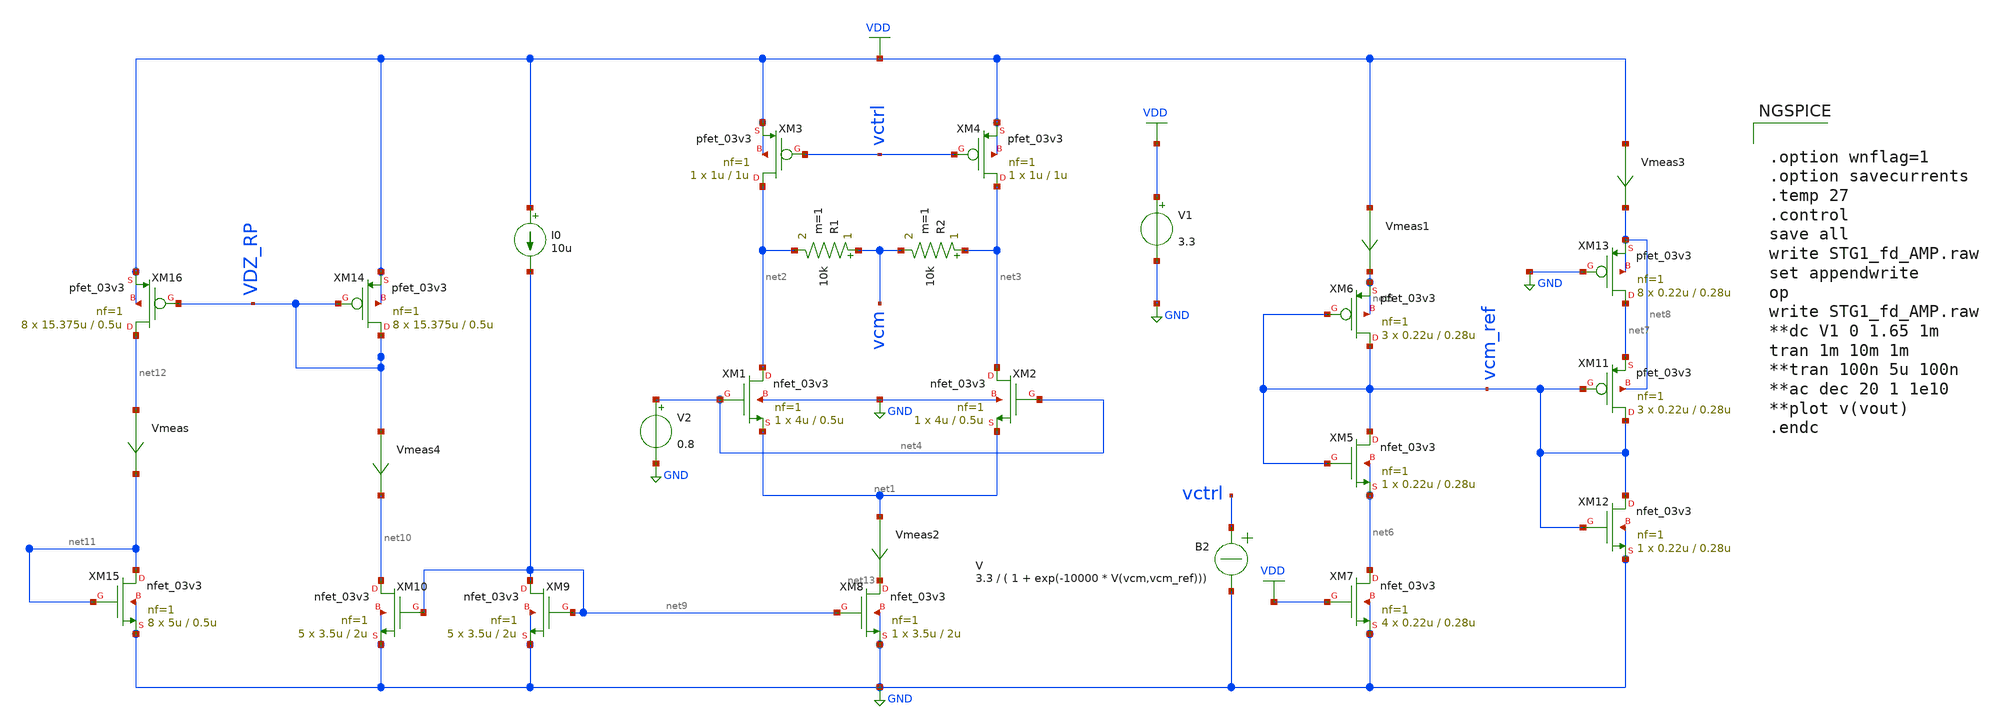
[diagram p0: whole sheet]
** sch_path: Design_Files/TB_ideal/STG1_fd_AMP.sch
**.subckt STG1_fd_AMP
XM1 net2 net4 net1 GND nfet_03v3 L=0.5u W=4u nf=1 ad='int((nf+1)/2) * W/nf * 0.18u' as='int((nf+2)/2) * W/nf * 0.18u'
+ pd='2*int((nf+1)/2) * (W/nf + 0.18u)' ps='2*int((nf+2)/2) * (W/nf + 0.18u)' nrd='0.18u / W' nrs='0.18u / W'
+ sa=0 sb=0 sd=0 m=1
XM2 net3 net4 net1 GND nfet_03v3 L=0.5u W=4u nf=1 ad='int((nf+1)/2) * W/nf * 0.18u' as='int((nf+2)/2) * W/nf * 0.18u'
+ pd='2*int((nf+1)/2) * (W/nf + 0.18u)' ps='2*int((nf+2)/2) * (W/nf + 0.18u)' nrd='0.18u / W' nrs='0.18u / W'
+ sa=0 sb=0 sd=0 m=1
XM3 net2 vctrl VDD VDD pfet_03v3 L=1u W=1u nf=1 ad='int((nf+1)/2) * W/nf * 0.18u' as='int((nf+2)/2) * W/nf * 0.18u'
+ pd='2*int((nf+1)/2) * (W/nf + 0.18u)' ps='2*int((nf+2)/2) * (W/nf + 0.18u)' nrd='0.18u / W' nrs='0.18u / W'
+ sa=0 sb=0 sd=0 m=1
XM4 net3 vctrl VDD VDD pfet_03v3 L=1u W=1u nf=1 ad='int((nf+1)/2) * W/nf * 0.18u' as='int((nf+2)/2) * W/nf * 0.18u'
+ pd='2*int((nf+1)/2) * (W/nf + 0.18u)' ps='2*int((nf+2)/2) * (W/nf + 0.18u)' nrd='0.18u / W' nrs='0.18u / W'
+ sa=0 sb=0 sd=0 m=1
R1 vcm net2 10k m=1
R2 net3 vcm 10k m=1
XM5 vcm_ref vcm_ref net6 net6 nfet_03v3 L=0.28u W=0.22u nf=1 ad='int((nf+1)/2) * W/nf * 0.18u' as='int((nf+2)/2) * W/nf * 0.18u'
+ pd='2*int((nf+1)/2) * (W/nf + 0.18u)' ps='2*int((nf+2)/2) * (W/nf + 0.18u)' nrd='0.18u / W' nrs='0.18u / W'
+ sa=0 sb=0 sd=0 m=1
XM6 vcm_ref vcm_ref net5 net5 pfet_03v3 L=0.28u W=0.22u nf=1 ad='int((nf+1)/2) * W/nf * 0.18u' as='int((nf+2)/2) * W/nf * 0.18u'
+ pd='2*int((nf+1)/2) * (W/nf + 0.18u)' ps='2*int((nf+2)/2) * (W/nf + 0.18u)' nrd='0.18u / W' nrs='0.18u / W'
+ sa=0 sb=0 sd=0 m=3
XM7 net6 VDD GND GND nfet_03v3 L=0.28u W=0.22u nf=1 ad='int((nf+1)/2) * W/nf * 0.18u' as='int((nf+2)/2) * W/nf * 0.18u'
+ pd='2*int((nf+1)/2) * (W/nf + 0.18u)' ps='2*int((nf+2)/2) * (W/nf + 0.18u)' nrd='0.18u / W' nrs='0.18u / W'
+ sa=0 sb=0 sd=0 m=4
V1 VDD GND 3.3
Vmeas1 VDD net5 0
.save i(vmeas1)
XM11 vcm_ref vcm_ref net7 net8 pfet_03v3 L=0.28u W=0.22u nf=1 ad='int((nf+1)/2) * W/nf * 0.18u' as='int((nf+2)/2) * W/nf * 0.18u'
+ pd='2*int((nf+1)/2) * (W/nf + 0.18u)' ps='2*int((nf+2)/2) * (W/nf + 0.18u)' nrd='0.18u / W' nrs='0.18u / W'
+ sa=0 sb=0 sd=0 m=3
XM12 vcm_ref vcm_ref GND GND nfet_03v3 L=0.28u W=0.22u nf=1 ad='int((nf+1)/2) * W/nf * 0.18u' as='int((nf+2)/2) * W/nf * 0.18u'
+ pd='2*int((nf+1)/2) * (W/nf + 0.18u)' ps='2*int((nf+2)/2) * (W/nf + 0.18u)' nrd='0.18u / W' nrs='0.18u / W'
+ sa=0 sb=0 sd=0 m=1
XM13 net7 GND net8 net8 pfet_03v3 L=0.28u W=0.22u nf=1 ad='int((nf+1)/2) * W/nf * 0.18u' as='int((nf+2)/2) * W/nf * 0.18u'
+ pd='2*int((nf+1)/2) * (W/nf + 0.18u)' ps='2*int((nf+2)/2) * (W/nf + 0.18u)' nrd='0.18u / W' nrs='0.18u / W'
+ sa=0 sb=0 sd=0 m=8
Vmeas3 VDD net8 0
.save i(vmeas3)
B2 vctrl GND V = 3.3 / ( 1 + exp(-10000 * V(vcm,vcm_ref)))
V2 net4 GND 0.8
XM8 net13 net9 GND GND nfet_03v3 L=2u W=3.5u nf=1 ad='int((nf+1)/2) * W/nf * 0.18u' as='int((nf+2)/2) * W/nf * 0.18u'
+ pd='2*int((nf+1)/2) * (W/nf + 0.18u)' ps='2*int((nf+2)/2) * (W/nf + 0.18u)' nrd='0.18u / W' nrs='0.18u / W'
+ sa=0 sb=0 sd=0 m=1
XM9 net9 net9 GND GND nfet_03v3 L=2u W=3.5u nf=1 ad='int((nf+1)/2) * W/nf * 0.18u' as='int((nf+2)/2) * W/nf * 0.18u'
+ pd='2*int((nf+1)/2) * (W/nf + 0.18u)' ps='2*int((nf+2)/2) * (W/nf + 0.18u)' nrd='0.18u / W' nrs='0.18u / W'
+ sa=0 sb=0 sd=0 m=5
I0 VDD net9 10u
Vmeas2 net1 net13 0
.save i(vmeas2)
XM10 net10 net9 GND GND nfet_03v3 L=2u W=3.5u nf=1 ad='int((nf+1)/2) * W/nf * 0.18u' as='int((nf+2)/2) * W/nf * 0.18u'
+ pd='2*int((nf+1)/2) * (W/nf + 0.18u)' ps='2*int((nf+2)/2) * (W/nf + 0.18u)' nrd='0.18u / W' nrs='0.18u / W'
+ sa=0 sb=0 sd=0 m=5
XM14 VDZ_RP VDZ_RP VDD VDD pfet_03v3 L=0.5u W=15.375u nf=1 ad='int((nf+1)/2) * W/nf * 0.18u' as='int((nf+2)/2) * W/nf * 0.18u'
+ pd='2*int((nf+1)/2) * (W/nf + 0.18u)' ps='2*int((nf+2)/2) * (W/nf + 0.18u)' nrd='0.18u / W' nrs='0.18u / W'
+ sa=0 sb=0 sd=0 m=8
Vmeas4 VDZ_RP net10 0
.save i(vmeas4)
XM15 net11 net11 GND GND nfet_03v3 L=0.5u W=5u nf=1 ad='int((nf+1)/2) * W/nf * 0.18u' as='int((nf+2)/2) * W/nf * 0.18u'
+ pd='2*int((nf+1)/2) * (W/nf + 0.18u)' ps='2*int((nf+2)/2) * (W/nf + 0.18u)' nrd='0.18u / W' nrs='0.18u / W'
+ sa=0 sb=0 sd=0 m=8
Vmeas net12 net11 0
.save i(vmeas)
XM16 net12 VDZ_RP VDD VDD pfet_03v3 L=0.5u W=15.375u nf=1 ad='int((nf+1)/2) * W/nf * 0.18u' as='int((nf+2)/2) * W/nf * 0.18u'
+ pd='2*int((nf+1)/2) * (W/nf + 0.18u)' ps='2*int((nf+2)/2) * (W/nf + 0.18u)' nrd='0.18u / W' nrs='0.18u / W'
+ sa=0 sb=0 sd=0 m=8
**** begin user architecture code


.option wnflag=1
.option savecurrents
.temp 27
.control
save all
write STG1_fd_AMP.raw
set appendwrite
op
write STG1_fd_AMP.raw
**dc V1 0 1.65 1m
tran 1m 10m 1m
**tran 100n 5u 100n
**ac dec 20 1 1e10
**plot v(vout)
.endc




.save @m.xm1.m0[gm]
.save @m.xm1.m0[id]
.save @m.xm1.m0[vth]
.save @m.xm1.m0[gds]
.save @m.xm1.m0[cgg]
.save @m.xm1.m0[cgs]
.save @m.xm1.m0[cgd]
.save @m.xm2.m0[gm]
.save @m.xm2.m0[id]
.save @m.xm2.m0[vth]
.save @m.xm2.m0[gds]
.save @m.xm2.m0[cgg]
.save @m.xm2.m0[cgs]
.save @m.xm2.m0[cgd]
.save @m.xm3.m0[gm]
.save @m.xm3.m0[id]
.save @m.xm3.m0[vth]
.save @m.xm3.m0[vds]
.save @m.xm3.m0[gds]
.save @m.xm3.m0[cgg]
.save @m.xm3.m0[cgs]
.save @m.xm3.m0[cgd]
.save @m.xm4.m0[gm]
.save @m.xm4.m0[id]
.save @m.xm4.m0[vth]
.save @m.xm4.m0[vds]
.save @m.xm4.m0[gds]
.save @m.xm4.m0[cgg]
.save @m.xm4.m0[cgs]
.save @m.xm4.m0[cgd]



.lib /foss/pdks/volare/gf180mcu/versions/0fe599b2afb6708d281543108caf8310912f54af/gf180mcuD/libs.tech/ngspice/sm141064.ngspice typical
.include /foss/pdks/volare/gf180mcu/versions/0fe599b2afb6708d281543108caf8310912f54af/gf180mcuD/libs.tech/ngspice/design.ngspice
.lib /foss/pdks/volare/gf180mcu/versions/0fe599b2afb6708d281543108caf8310912f54af/gf180mcuD/libs.tech/ngspice/sm141064.ngspice res_statistical

**.include $::180MCU_MODELS/design.ngspice
**.lib $::180MCU_MODELS/sm141064.ngspice typical
**.lib $::180MCU_MODELS/sm141064.ngspice res_typical
* .lib $::180MCU_MODELS/sm141064.ngspice res_statistical
*.include $::180MCU_MODELS/design.ngspice
*.lib $::180MCU_MODELS/sm141064.ngspice typical


**** end user architecture code
**.ends
.GLOBAL VDD
.GLOBAL GND
.end
